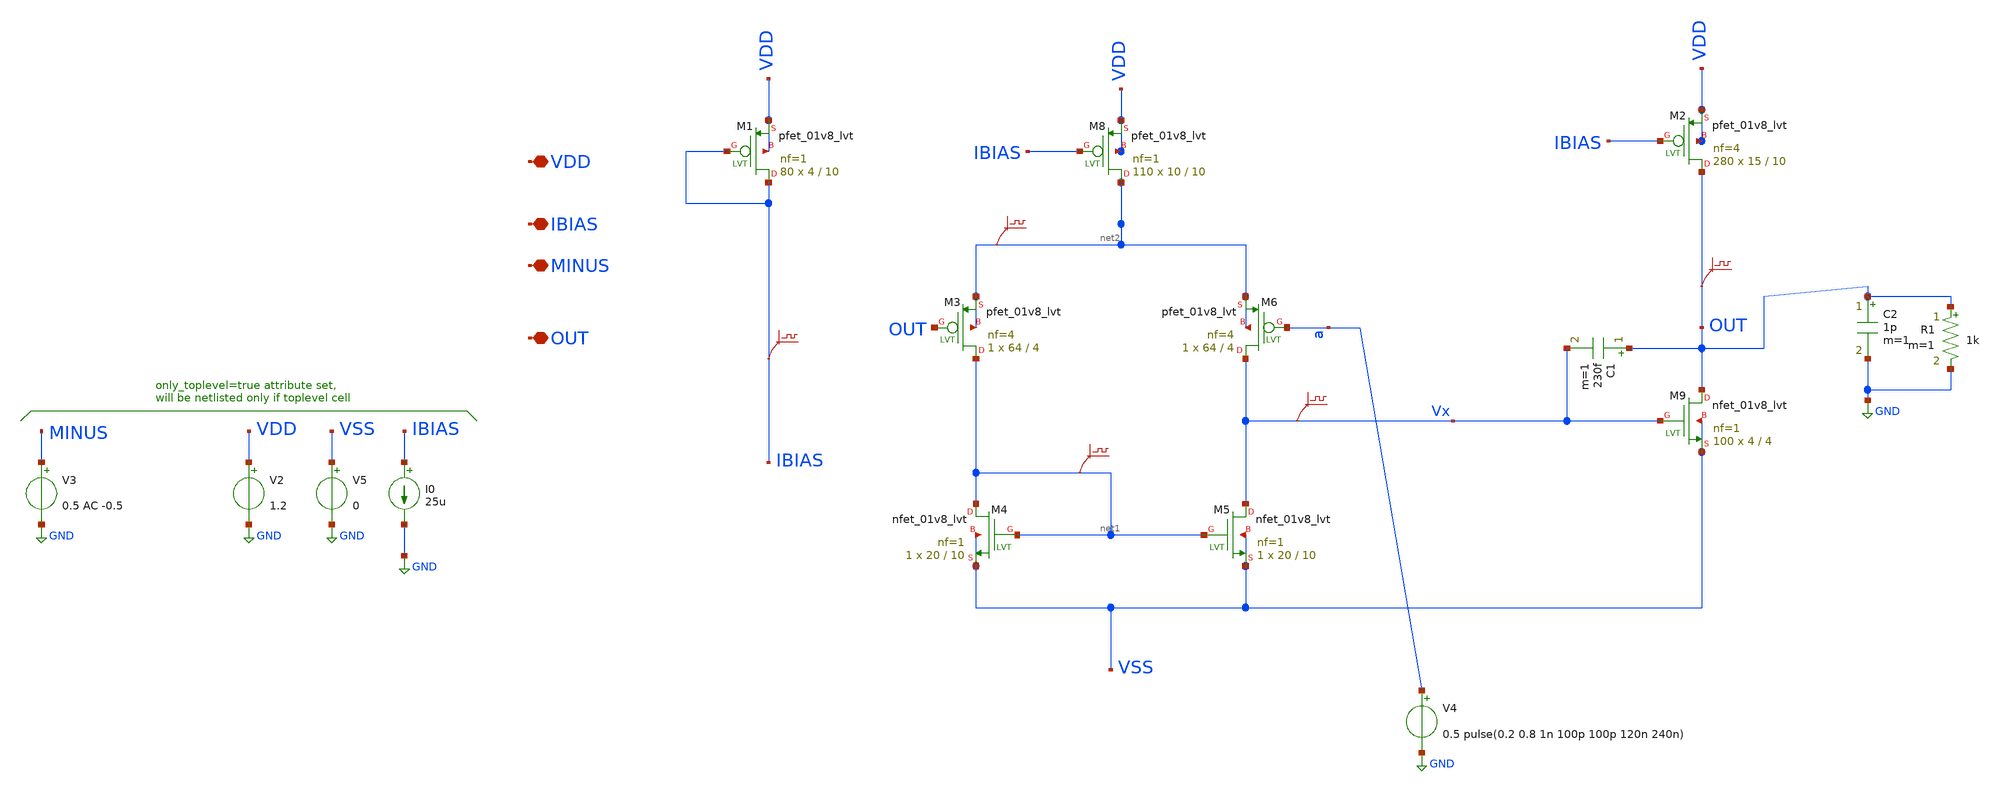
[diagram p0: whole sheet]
** sch_path: q2_opamp_settling_0.8patlama.sch
**.subckt q2_opamp_settling_0.8patlama VDD MINUS OUT IBIAS
*.iopin VDD
*.iopin MINUS
*.iopin OUT
*.iopin IBIAS
V3 MINUS GND 0.5 AC -0.5
V5 VSS GND 0
I0 IBIAS GND 25u
V2 VDD GND 1.2
.save v(vx)
XM4 net1 net1 VSS VSS sky130_fd_pr__nfet_01v8_lvt L=10 W=20 nf=1 ad='int((nf+1)/2) * W/nf * 0.29' as='int((nf+2)/2) * W/nf * 0.29'
+ pd='2*int((nf+1)/2) * (W/nf + 0.29)' ps='2*int((nf+2)/2) * (W/nf + 0.29)' nrd='0.29 / W' nrs='0.29 / W'
+ sa=0 sb=0 sd=0 mult=1 m=1
XM5 Vx net1 VSS VSS sky130_fd_pr__nfet_01v8_lvt L=10 W=20 nf=1 ad='int((nf+1)/2) * W/nf * 0.29' as='int((nf+2)/2) * W/nf * 0.29'
+ pd='2*int((nf+1)/2) * (W/nf + 0.29)' ps='2*int((nf+2)/2) * (W/nf + 0.29)' nrd='0.29 / W' nrs='0.29 / W'
+ sa=0 sb=0 sd=0 mult=1 m=1
XM3 net1 OUT net2 net2 sky130_fd_pr__pfet_01v8_lvt L=4 W=64 nf=4 ad='int((nf+1)/2) * W/nf * 0.29' as='int((nf+2)/2) * W/nf * 0.29'
+ pd='2*int((nf+1)/2) * (W/nf + 0.29)' ps='2*int((nf+2)/2) * (W/nf + 0.29)' nrd='0.29 / W' nrs='0.29 / W'
+ sa=0 sb=0 sd=0 mult=1 m=1
XM6 Vx a net2 net2 sky130_fd_pr__pfet_01v8_lvt L=4 W=64 nf=4 ad='int((nf+1)/2) * W/nf * 0.29' as='int((nf+2)/2) * W/nf * 0.29'
+ pd='2*int((nf+1)/2) * (W/nf + 0.29)' ps='2*int((nf+2)/2) * (W/nf + 0.29)' nrd='0.29 / W' nrs='0.29 / W'
+ sa=0 sb=0 sd=0 mult=1 m=1
.save v(net2)
XM9 OUT Vx VSS VSS sky130_fd_pr__nfet_01v8_lvt L=4 W=4 nf=1 ad='int((nf+1)/2) * W/nf * 0.29' as='int((nf+2)/2) * W/nf * 0.29'
+ pd='2*int((nf+1)/2) * (W/nf + 0.29)' ps='2*int((nf+2)/2) * (W/nf + 0.29)' nrd='0.29 / W' nrs='0.29 / W'
+ sa=0 sb=0 sd=0 mult=100 m=100
.save v(net1)
.save v(out)
.save v(ibias)
C1 OUT Vx 230f m=1
C2 OUT GND 1p m=1
R1 OUT GND 1k m=1
V4 a GND 0.5 pulse(0.2 0.8 1n 100p 100p 120n 240n)
XM1 IBIAS IBIAS VDD VDD sky130_fd_pr__pfet_01v8_lvt L=10 W=4 nf=1 ad='int((nf+1)/2) * W/nf * 0.29' as='int((nf+2)/2) * W/nf * 0.29'
+ pd='2*int((nf+1)/2) * (W/nf + 0.29)' ps='2*int((nf+2)/2) * (W/nf + 0.29)' nrd='0.29 / W' nrs='0.29 / W'
+ sa=0 sb=0 sd=0 mult=80 m=80
XM2 OUT IBIAS VDD VDD sky130_fd_pr__pfet_01v8_lvt L=10 W=15 nf=4 ad='int((nf+1)/2) * W/nf * 0.29' as='int((nf+2)/2) * W/nf * 0.29'
+ pd='2*int((nf+1)/2) * (W/nf + 0.29)' ps='2*int((nf+2)/2) * (W/nf + 0.29)' nrd='0.29 / W' nrs='0.29 / W'
+ sa=0 sb=0 sd=0 mult=280 m=280
XM8 net2 IBIAS VDD VDD sky130_fd_pr__pfet_01v8_lvt L=10 W=10 nf=1 ad='int((nf+1)/2) * W/nf * 0.29' as='int((nf+2)/2) * W/nf * 0.29'
+ pd='2*int((nf+1)/2) * (W/nf + 0.29)' ps='2*int((nf+2)/2) * (W/nf + 0.29)' nrd='0.29 / W' nrs='0.29 / W'
+ sa=0 sb=0 sd=0 mult=110 m=110
**** begin user architecture code

** opencircuitdesign pdks install
.lib $::SKYWATER_MODELS/sky130.lib.spice tt





.control

*ac dec 20 1 10g
*run
*plot db(v(out)) 180*cph(v(out))/pi
*plot db(v(Vx)) 180*cph(v(Vx))/pi
*reset
tran 0.01n 200n
plot out


save @m.xm5.msky130_fd_pr__nfet_01v8_lvt[gm]
save @m.xm5.msky130_fd_pr__nfet_01v8_lvt[vth]
save @m.xm5.msky130_fd_pr__nfet_01v8_lvt[vdsat]
save @m.xm5.msky130_fd_pr__nfet_01v8_lvt[vds]
save @m.xm5.msky130_fd_pr__nfet_01v8_lvt[id]
save @m.xm5.msky130_fd_pr__nfet_01v8_lvt[gds]

save @m.xm6.msky130_fd_pr__pfet_01v8_lvt[gm]
save @m.xm6.msky130_fd_pr__pfet_01v8_lvt[vth]
save @m.xm6.msky130_fd_pr__pfet_01v8_lvt[vdsat]
save @m.xm6.msky130_fd_pr__pfet_01v8_lvt[vds]
save @m.xm6.msky130_fd_pr__pfet_01v8_lvt[id]
save @m.xm6.msky130_fd_pr__pfet_01v8_lvt[gds]

save @m.xm9.msky130_fd_pr__nfet_01v8_lvt[gm]
save @m.xm9.msky130_fd_pr__nfet_01v8_lvt[vth]
save @m.xm9.msky130_fd_pr__nfet_01v8_lvt[vdsat]
save @m.xm9.msky130_fd_pr__nfet_01v8_lvt[vds]
save @m.xm9.msky130_fd_pr__nfet_01v8_lvt[id]
save @m.xm9.msky130_fd_pr__nfet_01v8_lvt[gds]

save @m.xm10.msky130_fd_pr__pfet_01v8_lvt[gm]
save @m.xm10.msky130_fd_pr__pfet_01v8_lvt[vth]
save @m.xm10.msky130_fd_pr__pfet_01v8_lvt[vdsat]
save @m.xm10.msky130_fd_pr__pfet_01v8_lvt[vds]
save @m.xm10.msky130_fd_pr__pfet_01v8_lvt[id]
save @m.xm10.msky130_fd_pr__pfet_01v8_lvt[gds]

save @m.xm11.msky130_fd_pr__pfet_01v8_lvt[gm]
save @m.xm11.msky130_fd_pr__pfet_01v8_lvt[vth]
save @m.xm11.msky130_fd_pr__pfet_01v8_lvt[vdsat]
save @m.xm11.msky130_fd_pr__pfet_01v8_lvt[vds]
save @m.xm11.msky130_fd_pr__pfet_01v8_lvt[id]
save @m.xm11.msky130_fd_pr__pfet_01v8_lvt[gds]


save all
op

write q2_opamp_settling_0.8patlama.raw

.endc


**** end user architecture code
**.ends
.GLOBAL GND
.end
